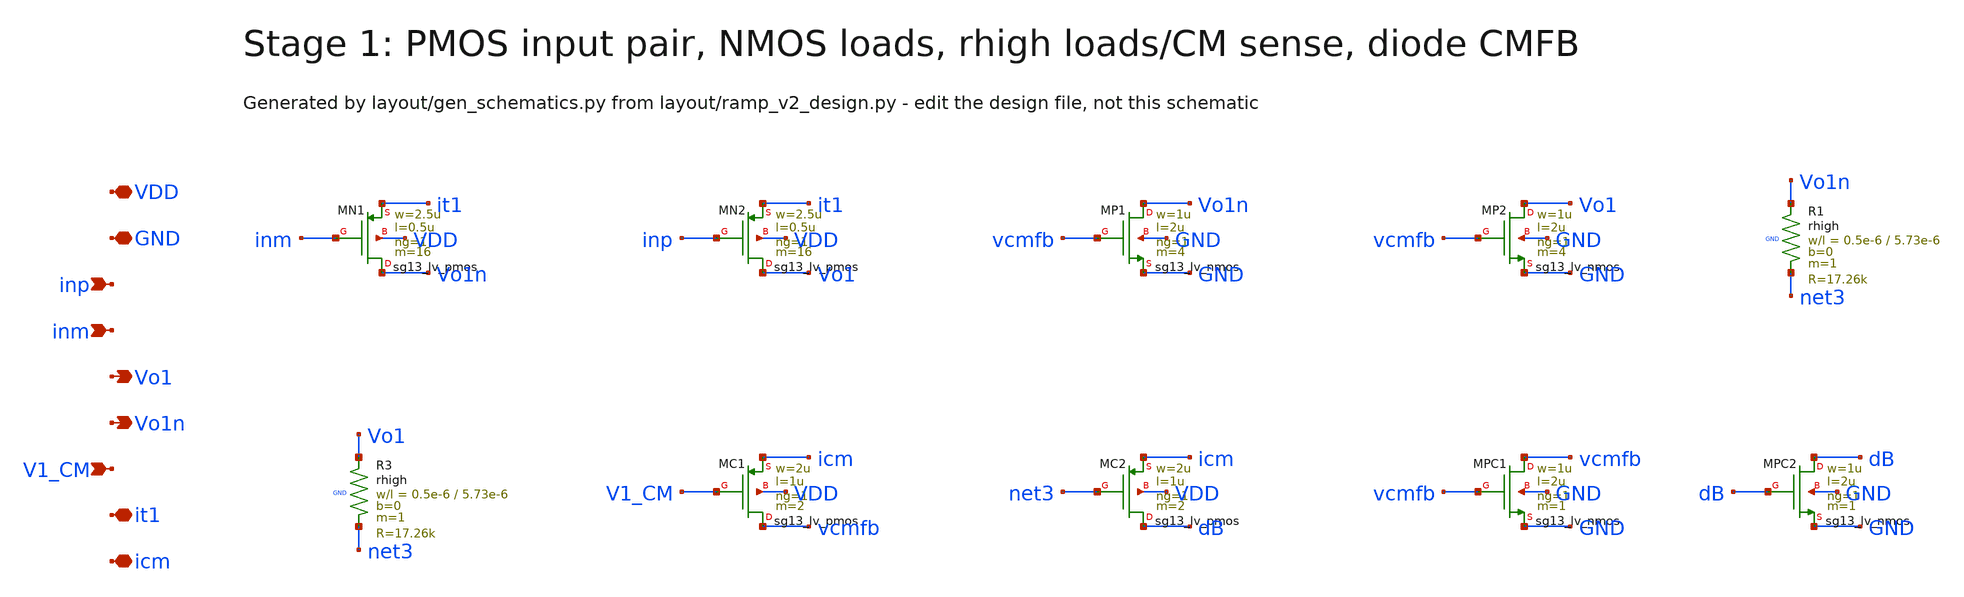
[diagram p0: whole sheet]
** sch_path: Design Files/RAMP/RAMP-V2/STG1_V2.sch
**.subckt STG1_V2 VDD GND inp inm Vo1 Vo1n V1_CM it1 icm
*.iopin VDD
*.iopin GND
*.ipin inp
*.ipin inm
*.opin Vo1
*.opin Vo1n
*.ipin V1_CM
*.iopin it1
*.iopin icm
XMN1 Vo1n inm it1 VDD sg13_lv_pmos w=2.5u l=0.5u ng=1 m=16 mm_ok=1
XMN2 Vo1 inp it1 VDD sg13_lv_pmos w=2.5u l=0.5u ng=1 m=16 mm_ok=1
XMP1 Vo1n vcmfb GND GND sg13_lv_nmos w=1u l=2u ng=1 m=4 mm_ok=1
XMP2 Vo1 vcmfb GND GND sg13_lv_nmos w=1u l=2u ng=1 m=4 mm_ok=1
XR1 Vo1n net3 GND rhigh w=0.5e-6 l=5.73e-6 m=1 b=0 mm_ok=1
XR3 Vo1 net3 GND rhigh w=0.5e-6 l=5.73e-6 m=1 b=0 mm_ok=1
XMC1 vcmfb V1_CM icm VDD sg13_lv_pmos w=2u l=1u ng=1 m=2 mm_ok=1
XMC2 dB net3 icm VDD sg13_lv_pmos w=2u l=1u ng=1 m=2 mm_ok=1
XMPC1 vcmfb vcmfb GND GND sg13_lv_nmos w=1u l=2u ng=1 m=1 mm_ok=1
XMPC2 dB dB GND GND sg13_lv_nmos w=1u l=2u ng=1 m=1 mm_ok=1
**.ends
.end
